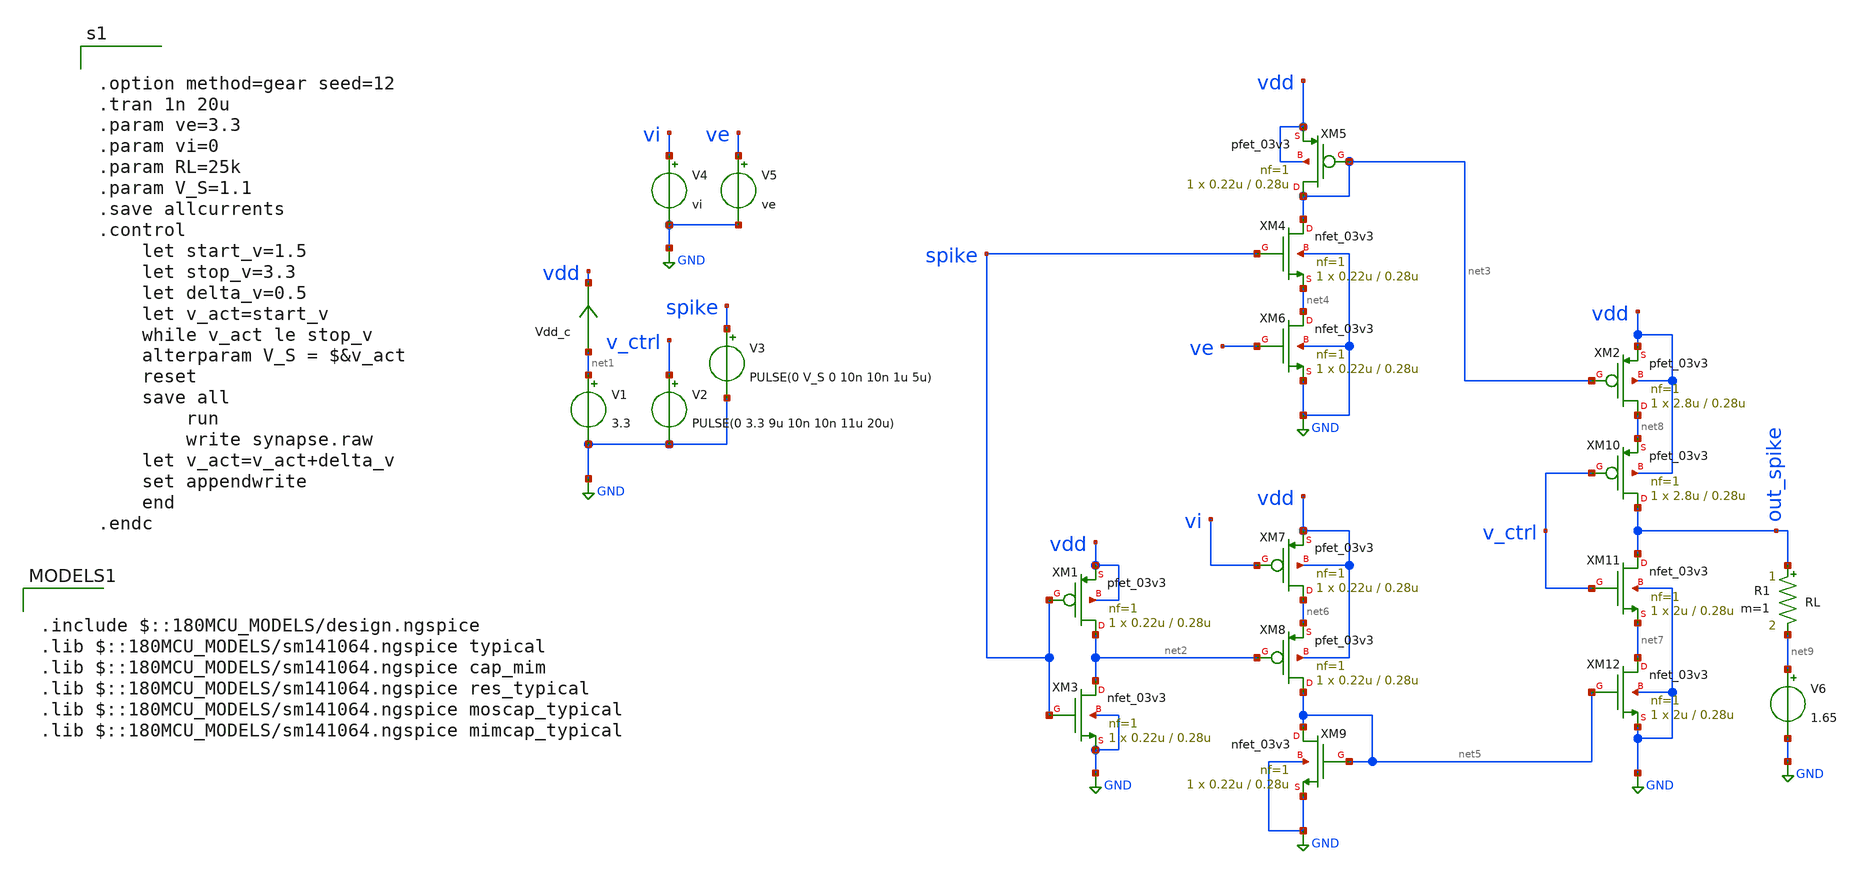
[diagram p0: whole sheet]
** sch_path: designs/libs/tb_synapse/synapse.sch
**.subckt synapse
V1 net1 GND 3.3
Vdd_c net1 vdd 0
.save i(vdd_c)
XM5 net3 net3 vdd vdd pfet_03v3 L=0.28u W=0.22u nf=1 ad='int((nf+1)/2) * W/nf * 0.18u' as='int((nf+2)/2) * W/nf * 0.18u'
+ pd='2*int((nf+1)/2) * (W/nf + 0.18u)' ps='2*int((nf+2)/2) * (W/nf + 0.18u)' nrd='0.18u / W' nrs='0.18u / W'
+ sa=0 sb=0 sd=0 m=1
XM1 net2 spike vdd vdd pfet_03v3 L=0.28u W=0.22u nf=1 ad='int((nf+1)/2) * W/nf * 0.18u' as='int((nf+2)/2) * W/nf * 0.18u'
+ pd='2*int((nf+1)/2) * (W/nf + 0.18u)' ps='2*int((nf+2)/2) * (W/nf + 0.18u)' nrd='0.18u / W' nrs='0.18u / W'
+ sa=0 sb=0 sd=0 m=1
XM3 net2 spike GND GND nfet_03v3 L=0.28u W=0.22u nf=1 ad='int((nf+1)/2) * W/nf * 0.18u' as='int((nf+2)/2) * W/nf * 0.18u'
+ pd='2*int((nf+1)/2) * (W/nf + 0.18u)' ps='2*int((nf+2)/2) * (W/nf + 0.18u)' nrd='0.18u / W' nrs='0.18u / W'
+ sa=0 sb=0 sd=0 m=1
XM4 net3 spike net4 GND nfet_03v3 L=0.28u W=0.22u nf=1 ad='int((nf+1)/2) * W/nf * 0.18u' as='int((nf+2)/2) * W/nf * 0.18u'
+ pd='2*int((nf+1)/2) * (W/nf + 0.18u)' ps='2*int((nf+2)/2) * (W/nf + 0.18u)' nrd='0.18u / W' nrs='0.18u / W'
+ sa=0 sb=0 sd=0 m=1
XM6 net4 ve GND GND nfet_03v3 L=0.28u W=0.22u nf=1 ad='int((nf+1)/2) * W/nf * 0.18u' as='int((nf+2)/2) * W/nf * 0.18u'
+ pd='2*int((nf+1)/2) * (W/nf + 0.18u)' ps='2*int((nf+2)/2) * (W/nf + 0.18u)' nrd='0.18u / W' nrs='0.18u / W'
+ sa=0 sb=0 sd=0 m=1
XM7 net6 vi vdd vdd pfet_03v3 L=0.28u W=0.22u nf=1 ad='int((nf+1)/2) * W/nf * 0.18u' as='int((nf+2)/2) * W/nf * 0.18u'
+ pd='2*int((nf+1)/2) * (W/nf + 0.18u)' ps='2*int((nf+2)/2) * (W/nf + 0.18u)' nrd='0.18u / W' nrs='0.18u / W'
+ sa=0 sb=0 sd=0 m=1
XM8 net5 net2 net6 vdd pfet_03v3 L=0.28u W=0.22u nf=1 ad='int((nf+1)/2) * W/nf * 0.18u' as='int((nf+2)/2) * W/nf * 0.18u'
+ pd='2*int((nf+1)/2) * (W/nf + 0.18u)' ps='2*int((nf+2)/2) * (W/nf + 0.18u)' nrd='0.18u / W' nrs='0.18u / W'
+ sa=0 sb=0 sd=0 m=1
XM9 net5 net5 GND GND nfet_03v3 L=0.28u W=0.22u nf=1 ad='int((nf+1)/2) * W/nf * 0.18u' as='int((nf+2)/2) * W/nf * 0.18u'
+ pd='2*int((nf+1)/2) * (W/nf + 0.18u)' ps='2*int((nf+2)/2) * (W/nf + 0.18u)' nrd='0.18u / W' nrs='0.18u / W'
+ sa=0 sb=0 sd=0 m=1
XM2 net8 net3 vdd vdd pfet_03v3 L=0.28u W=2.8u nf=1 ad='int((nf+1)/2) * W/nf * 0.18u' as='int((nf+2)/2) * W/nf * 0.18u'
+ pd='2*int((nf+1)/2) * (W/nf + 0.18u)' ps='2*int((nf+2)/2) * (W/nf + 0.18u)' nrd='0.18u / W' nrs='0.18u / W'
+ sa=0 sb=0 sd=0 m=1
XM10 out_spike v_ctrl net8 vdd pfet_03v3 L=0.28u W=2.8u nf=1 ad='int((nf+1)/2) * W/nf * 0.18u' as='int((nf+2)/2) * W/nf * 0.18u'
+ pd='2*int((nf+1)/2) * (W/nf + 0.18u)' ps='2*int((nf+2)/2) * (W/nf + 0.18u)' nrd='0.18u / W' nrs='0.18u / W'
+ sa=0 sb=0 sd=0 m=1
XM11 out_spike v_ctrl net7 GND nfet_03v3 L=0.28u W=2u nf=1 ad='int((nf+1)/2) * W/nf * 0.18u' as='int((nf+2)/2) * W/nf * 0.18u'
+ pd='2*int((nf+1)/2) * (W/nf + 0.18u)' ps='2*int((nf+2)/2) * (W/nf + 0.18u)' nrd='0.18u / W' nrs='0.18u / W'
+ sa=0 sb=0 sd=0 m=1
XM12 net7 net5 GND GND nfet_03v3 L=0.28u W=2u nf=1 ad='int((nf+1)/2) * W/nf * 0.18u' as='int((nf+2)/2) * W/nf * 0.18u'
+ pd='2*int((nf+1)/2) * (W/nf + 0.18u)' ps='2*int((nf+2)/2) * (W/nf + 0.18u)' nrd='0.18u / W' nrs='0.18u / W'
+ sa=0 sb=0 sd=0 m=1
V2 v_ctrl GND PULSE(0 3.3 9u 10n 10n 11u 20u)
V3 spike GND PULSE(0 V_S 0 10n 10n 1u 5u)
V4 vi GND vi
V5 ve GND ve
V6 net9 GND 1.65
R1 out_spike net9 RL m=1
**** begin user architecture code


.option method=gear seed=12
.tran 1n 20u
.param ve=3.3
.param vi=0
.param RL=25k
.param V_S=1.1
.save allcurrents
.control
    let start_v=1.5
    let stop_v=3.3
    let delta_v=0.5
    let v_act=start_v
    while v_act le stop_v
	alterparam V_S = $&v_act
	reset
	save all
        run
        write synapse.raw
	let v_act=v_act+delta_v
	set appendwrite
    end
.endc



.include $::180MCU_MODELS/design.ngspice
.lib $::180MCU_MODELS/sm141064.ngspice typical
.lib $::180MCU_MODELS/sm141064.ngspice cap_mim
.lib $::180MCU_MODELS/sm141064.ngspice res_typical
.lib $::180MCU_MODELS/sm141064.ngspice moscap_typical
.lib $::180MCU_MODELS/sm141064.ngspice mimcap_typical

**** end user architecture code
**.ends
.GLOBAL GND
.end
